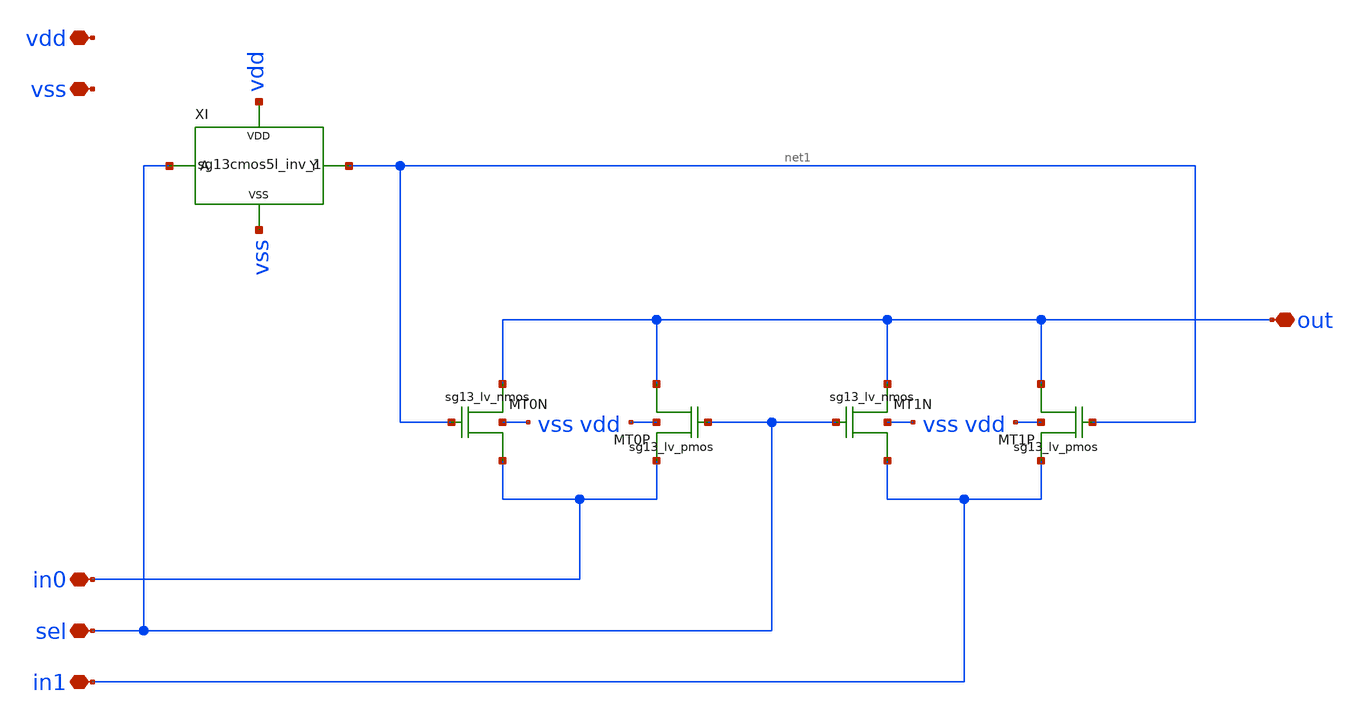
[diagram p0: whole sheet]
** sch_path: xschem/logic_gates/MUXLV.sch
**.subckt MUXLV out in0 in1 sel vdd vss
*.iopin out
*.iopin in0
*.iopin in1
*.iopin sel
*.iopin vdd
*.iopin vss
XMT0N out net1 in0 vss sg13_lv_nmos w=1.0u l=0.13u ng=1 m=1
XMT0P in0 sel out vdd sg13_lv_pmos w=2.0u l=0.13u ng=1 m=1
XMT1N out sel in1 vss sg13_lv_nmos w=1.0u l=0.13u ng=1 m=1
XMT1P in1 net1 out vdd sg13_lv_pmos w=2.0u l=0.13u ng=1 m=1
XI net1 sel vdd vss sg13cmos5l_inv_1
**.ends

* expanding   symbol:  logic_gates/sg13cmos5l_inv_1.sym # of pins=4
** sym_path: xschem/logic_gates/sg13cmos5l_inv_1.sym
** sch_path: xschem/logic_gates/sg13cmos5l_inv_1.sch
.subckt sg13cmos5l_inv_1 Y A VDD VSS
*.iopin Y
*.iopin A
*.iopin VDD
*.iopin VSS
XMN0 Y A VSS VSS sg13_lv_nmos w=0.74u l=0.13u ng=1 m=1
XMP0 VDD A Y VDD sg13_lv_pmos w=1.12u l=0.13u ng=1 m=1
.ends

.end
